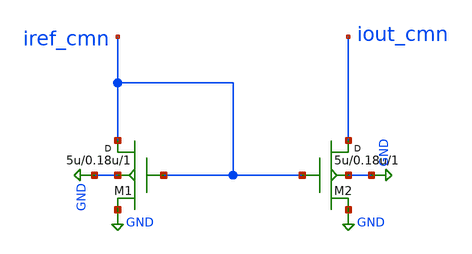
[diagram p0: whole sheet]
** sch_path: synthetic/blocks/current_mirror_nmos.sch
**.subckt current_mirror_nmos
M1 iref_cmn iref_cmn GND GND nmos w=5u l=0.18u m=1
M2 iout_cmn iref_cmn GND GND nmos w=5u l=0.18u m=1
**.ends
.GLOBAL GND
.end
